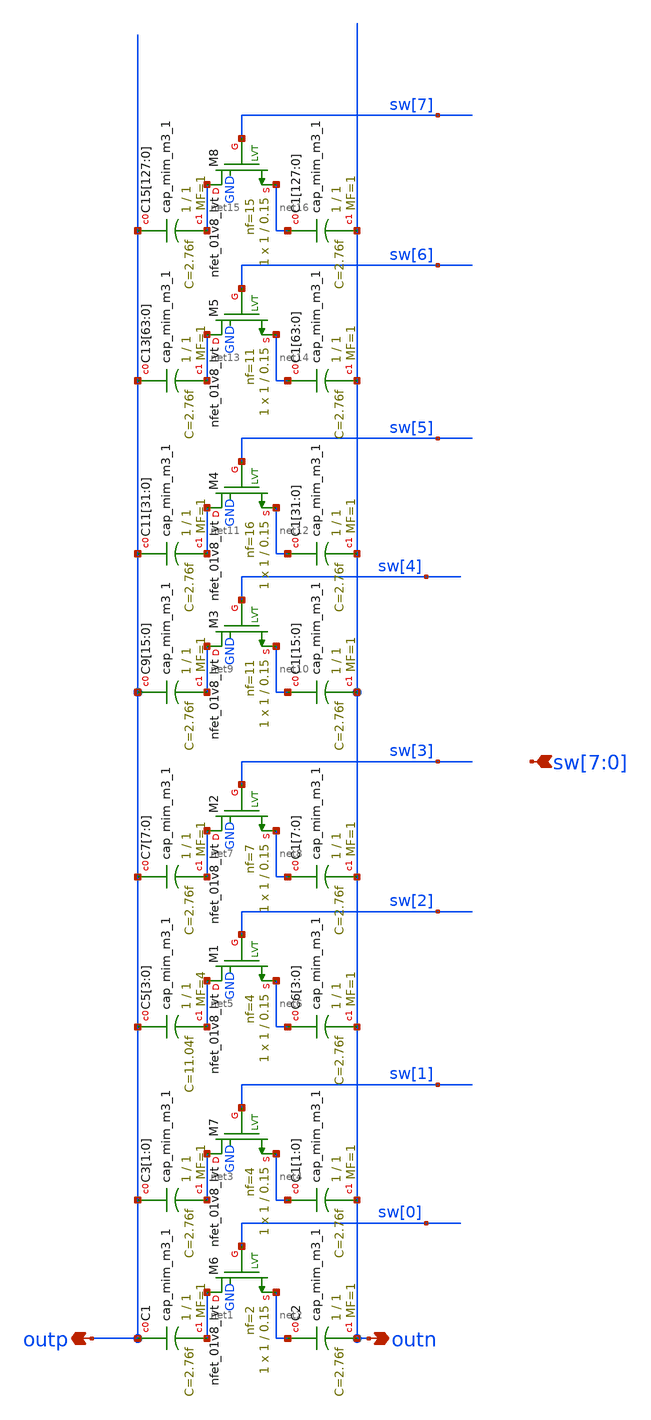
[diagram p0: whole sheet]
** sch_path: generators/lc-dco/xschem_rundir/mim_1m2C.sch
**.subckt mim_1m2C outn outp sw[7],sw[6],sw[5],sw[4],sw[3],sw[2],sw[1],sw[0]
*.opin outn
*.opin outp
*.ipin sw[7],sw[6],sw[5],sw[4],sw[3],sw[2],sw[1],sw[0]
XC1 outp net1 sky130_fd_pr__cap_mim_m3_1 W=1 L=1 MF=1 m=1
XC2 net2 outn sky130_fd_pr__cap_mim_m3_1 W=1 L=1 MF=1 m=1
XM6 net1 sw[0] net2 GND sky130_fd_pr__nfet_01v8_lvt L=0.15 W=1 nf=2 ad='int((nf+1)/2) * W/nf * 0.29'
+ as='int((nf+2)/2) * W/nf * 0.29' pd='2*int((nf+1)/2) * (W/nf + 0.29)' ps='2*int((nf+2)/2) * (W/nf + 0.29)'
+ nrd='0.29 / W' nrs='0.29 / W' sa=0 sb=0 sd=0 mult=1 m=1
XC3[1] outp net3 sky130_fd_pr__cap_mim_m3_1 W=1 L=1 MF=1 m=1
XC3[0] outp net3 sky130_fd_pr__cap_mim_m3_1 W=1 L=1 MF=1 m=1
XC1[1] net4 outn sky130_fd_pr__cap_mim_m3_1 W=1 L=1 MF=1 m=1
XC1[0] net4 outn sky130_fd_pr__cap_mim_m3_1 W=1 L=1 MF=1 m=1
XM7 net3 sw[1] net4 GND sky130_fd_pr__nfet_01v8_lvt L=0.15 W=1 nf=4 ad='int((nf+1)/2) * W/nf * 0.29'
+ as='int((nf+2)/2) * W/nf * 0.29' pd='2*int((nf+1)/2) * (W/nf + 0.29)' ps='2*int((nf+2)/2) * (W/nf + 0.29)'
+ nrd='0.29 / W' nrs='0.29 / W' sa=0 sb=0 sd=0 mult=1 m=1
XC5[3] outp net5 sky130_fd_pr__cap_mim_m3_1 W=1 L=1 MF=4 m=4
XC5[2] outp net5 sky130_fd_pr__cap_mim_m3_1 W=1 L=1 MF=4 m=4
XC5[1] outp net5 sky130_fd_pr__cap_mim_m3_1 W=1 L=1 MF=4 m=4
XC5[0] outp net5 sky130_fd_pr__cap_mim_m3_1 W=1 L=1 MF=4 m=4
XC6[3] net6 outn sky130_fd_pr__cap_mim_m3_1 W=1 L=1 MF=1 m=1
XC6[2] net6 outn sky130_fd_pr__cap_mim_m3_1 W=1 L=1 MF=1 m=1
XC6[1] net6 outn sky130_fd_pr__cap_mim_m3_1 W=1 L=1 MF=1 m=1
XC6[0] net6 outn sky130_fd_pr__cap_mim_m3_1 W=1 L=1 MF=1 m=1
XM1 net5 sw[2] net6 GND sky130_fd_pr__nfet_01v8_lvt L=0.15 W=1 nf=4 ad='int((nf+1)/2) * W/nf * 0.29'
+ as='int((nf+2)/2) * W/nf * 0.29' pd='2*int((nf+1)/2) * (W/nf + 0.29)' ps='2*int((nf+2)/2) * (W/nf + 0.29)'
+ nrd='0.29 / W' nrs='0.29 / W' sa=0 sb=0 sd=0 mult=1 m=1
XC7[7] outp net7 sky130_fd_pr__cap_mim_m3_1 W=1 L=1 MF=1 m=1
XC7[6] outp net7 sky130_fd_pr__cap_mim_m3_1 W=1 L=1 MF=1 m=1
XC7[5] outp net7 sky130_fd_pr__cap_mim_m3_1 W=1 L=1 MF=1 m=1
XC7[4] outp net7 sky130_fd_pr__cap_mim_m3_1 W=1 L=1 MF=1 m=1
XC7[3] outp net7 sky130_fd_pr__cap_mim_m3_1 W=1 L=1 MF=1 m=1
XC7[2] outp net7 sky130_fd_pr__cap_mim_m3_1 W=1 L=1 MF=1 m=1
XC7[1] outp net7 sky130_fd_pr__cap_mim_m3_1 W=1 L=1 MF=1 m=1
XC7[0] outp net7 sky130_fd_pr__cap_mim_m3_1 W=1 L=1 MF=1 m=1
XC1[7] net8 outn sky130_fd_pr__cap_mim_m3_1 W=1 L=1 MF=1 m=1
XC1[6] net8 outn sky130_fd_pr__cap_mim_m3_1 W=1 L=1 MF=1 m=1
XC1[5] net8 outn sky130_fd_pr__cap_mim_m3_1 W=1 L=1 MF=1 m=1
XC1[4] net8 outn sky130_fd_pr__cap_mim_m3_1 W=1 L=1 MF=1 m=1
XC1[3] net8 outn sky130_fd_pr__cap_mim_m3_1 W=1 L=1 MF=1 m=1
XC1[2] net8 outn sky130_fd_pr__cap_mim_m3_1 W=1 L=1 MF=1 m=1
XC1[1] net8 outn sky130_fd_pr__cap_mim_m3_1 W=1 L=1 MF=1 m=1
XC1[0] net8 outn sky130_fd_pr__cap_mim_m3_1 W=1 L=1 MF=1 m=1
XM2 net7 sw[3] net8 GND sky130_fd_pr__nfet_01v8_lvt L=0.15 W=1 nf=7 ad='int((nf+1)/2) * W/nf * 0.29'
+ as='int((nf+2)/2) * W/nf * 0.29' pd='2*int((nf+1)/2) * (W/nf + 0.29)' ps='2*int((nf+2)/2) * (W/nf + 0.29)'
+ nrd='0.29 / W' nrs='0.29 / W' sa=0 sb=0 sd=0 mult=1 m=1
XC9[15] outp net9 sky130_fd_pr__cap_mim_m3_1 W=1 L=1 MF=1 m=1
XC9[14] outp net9 sky130_fd_pr__cap_mim_m3_1 W=1 L=1 MF=1 m=1
XC9[13] outp net9 sky130_fd_pr__cap_mim_m3_1 W=1 L=1 MF=1 m=1
XC9[12] outp net9 sky130_fd_pr__cap_mim_m3_1 W=1 L=1 MF=1 m=1
XC9[11] outp net9 sky130_fd_pr__cap_mim_m3_1 W=1 L=1 MF=1 m=1
XC9[10] outp net9 sky130_fd_pr__cap_mim_m3_1 W=1 L=1 MF=1 m=1
XC9[9] outp net9 sky130_fd_pr__cap_mim_m3_1 W=1 L=1 MF=1 m=1
XC9[8] outp net9 sky130_fd_pr__cap_mim_m3_1 W=1 L=1 MF=1 m=1
XC9[7] outp net9 sky130_fd_pr__cap_mim_m3_1 W=1 L=1 MF=1 m=1
XC9[6] outp net9 sky130_fd_pr__cap_mim_m3_1 W=1 L=1 MF=1 m=1
XC9[5] outp net9 sky130_fd_pr__cap_mim_m3_1 W=1 L=1 MF=1 m=1
XC9[4] outp net9 sky130_fd_pr__cap_mim_m3_1 W=1 L=1 MF=1 m=1
XC9[3] outp net9 sky130_fd_pr__cap_mim_m3_1 W=1 L=1 MF=1 m=1
XC9[2] outp net9 sky130_fd_pr__cap_mim_m3_1 W=1 L=1 MF=1 m=1
XC9[1] outp net9 sky130_fd_pr__cap_mim_m3_1 W=1 L=1 MF=1 m=1
XC9[0] outp net9 sky130_fd_pr__cap_mim_m3_1 W=1 L=1 MF=1 m=1
XC1[15] net10 outn sky130_fd_pr__cap_mim_m3_1 W=1 L=1 MF=1 m=1
XC1[14] net10 outn sky130_fd_pr__cap_mim_m3_1 W=1 L=1 MF=1 m=1
XC1[13] net10 outn sky130_fd_pr__cap_mim_m3_1 W=1 L=1 MF=1 m=1
XC1[12] net10 outn sky130_fd_pr__cap_mim_m3_1 W=1 L=1 MF=1 m=1
XC1[11] net10 outn sky130_fd_pr__cap_mim_m3_1 W=1 L=1 MF=1 m=1
XC1[10] net10 outn sky130_fd_pr__cap_mim_m3_1 W=1 L=1 MF=1 m=1
XC1[9] net10 outn sky130_fd_pr__cap_mim_m3_1 W=1 L=1 MF=1 m=1
XC1[8] net10 outn sky130_fd_pr__cap_mim_m3_1 W=1 L=1 MF=1 m=1
XC1[7] net10 outn sky130_fd_pr__cap_mim_m3_1 W=1 L=1 MF=1 m=1
XC1[6] net10 outn sky130_fd_pr__cap_mim_m3_1 W=1 L=1 MF=1 m=1
XC1[5] net10 outn sky130_fd_pr__cap_mim_m3_1 W=1 L=1 MF=1 m=1
XC1[4] net10 outn sky130_fd_pr__cap_mim_m3_1 W=1 L=1 MF=1 m=1
XC1[3] net10 outn sky130_fd_pr__cap_mim_m3_1 W=1 L=1 MF=1 m=1
XC1[2] net10 outn sky130_fd_pr__cap_mim_m3_1 W=1 L=1 MF=1 m=1
XC1[1] net10 outn sky130_fd_pr__cap_mim_m3_1 W=1 L=1 MF=1 m=1
XC1[0] net10 outn sky130_fd_pr__cap_mim_m3_1 W=1 L=1 MF=1 m=1
XM3 net9 sw[4] net10 GND sky130_fd_pr__nfet_01v8_lvt L=0.15 W=1 nf=11 ad='int((nf+1)/2) * W/nf * 0.29'
+ as='int((nf+2)/2) * W/nf * 0.29' pd='2*int((nf+1)/2) * (W/nf + 0.29)' ps='2*int((nf+2)/2) * (W/nf + 0.29)'
+ nrd='0.29 / W' nrs='0.29 / W' sa=0 sb=0 sd=0 mult=1 m=1
XC11[31] outp net11 sky130_fd_pr__cap_mim_m3_1 W=1 L=1 MF=1 m=1
XC11[30] outp net11 sky130_fd_pr__cap_mim_m3_1 W=1 L=1 MF=1 m=1
XC11[29] outp net11 sky130_fd_pr__cap_mim_m3_1 W=1 L=1 MF=1 m=1
XC11[28] outp net11 sky130_fd_pr__cap_mim_m3_1 W=1 L=1 MF=1 m=1
XC11[27] outp net11 sky130_fd_pr__cap_mim_m3_1 W=1 L=1 MF=1 m=1
XC11[26] outp net11 sky130_fd_pr__cap_mim_m3_1 W=1 L=1 MF=1 m=1
XC11[25] outp net11 sky130_fd_pr__cap_mim_m3_1 W=1 L=1 MF=1 m=1
XC11[24] outp net11 sky130_fd_pr__cap_mim_m3_1 W=1 L=1 MF=1 m=1
XC11[23] outp net11 sky130_fd_pr__cap_mim_m3_1 W=1 L=1 MF=1 m=1
XC11[22] outp net11 sky130_fd_pr__cap_mim_m3_1 W=1 L=1 MF=1 m=1
XC11[21] outp net11 sky130_fd_pr__cap_mim_m3_1 W=1 L=1 MF=1 m=1
XC11[20] outp net11 sky130_fd_pr__cap_mim_m3_1 W=1 L=1 MF=1 m=1
XC11[19] outp net11 sky130_fd_pr__cap_mim_m3_1 W=1 L=1 MF=1 m=1
XC11[18] outp net11 sky130_fd_pr__cap_mim_m3_1 W=1 L=1 MF=1 m=1
XC11[17] outp net11 sky130_fd_pr__cap_mim_m3_1 W=1 L=1 MF=1 m=1
XC11[16] outp net11 sky130_fd_pr__cap_mim_m3_1 W=1 L=1 MF=1 m=1
XC11[15] outp net11 sky130_fd_pr__cap_mim_m3_1 W=1 L=1 MF=1 m=1
XC11[14] outp net11 sky130_fd_pr__cap_mim_m3_1 W=1 L=1 MF=1 m=1
XC11[13] outp net11 sky130_fd_pr__cap_mim_m3_1 W=1 L=1 MF=1 m=1
XC11[12] outp net11 sky130_fd_pr__cap_mim_m3_1 W=1 L=1 MF=1 m=1
XC11[11] outp net11 sky130_fd_pr__cap_mim_m3_1 W=1 L=1 MF=1 m=1
XC11[10] outp net11 sky130_fd_pr__cap_mim_m3_1 W=1 L=1 MF=1 m=1
XC11[9] outp net11 sky130_fd_pr__cap_mim_m3_1 W=1 L=1 MF=1 m=1
XC11[8] outp net11 sky130_fd_pr__cap_mim_m3_1 W=1 L=1 MF=1 m=1
XC11[7] outp net11 sky130_fd_pr__cap_mim_m3_1 W=1 L=1 MF=1 m=1
XC11[6] outp net11 sky130_fd_pr__cap_mim_m3_1 W=1 L=1 MF=1 m=1
XC11[5] outp net11 sky130_fd_pr__cap_mim_m3_1 W=1 L=1 MF=1 m=1
XC11[4] outp net11 sky130_fd_pr__cap_mim_m3_1 W=1 L=1 MF=1 m=1
XC11[3] outp net11 sky130_fd_pr__cap_mim_m3_1 W=1 L=1 MF=1 m=1
XC11[2] outp net11 sky130_fd_pr__cap_mim_m3_1 W=1 L=1 MF=1 m=1
XC11[1] outp net11 sky130_fd_pr__cap_mim_m3_1 W=1 L=1 MF=1 m=1
XC11[0] outp net11 sky130_fd_pr__cap_mim_m3_1 W=1 L=1 MF=1 m=1
XC1[31] net12 outn sky130_fd_pr__cap_mim_m3_1 W=1 L=1 MF=1 m=1
XC1[30] net12 outn sky130_fd_pr__cap_mim_m3_1 W=1 L=1 MF=1 m=1
XC1[29] net12 outn sky130_fd_pr__cap_mim_m3_1 W=1 L=1 MF=1 m=1
XC1[28] net12 outn sky130_fd_pr__cap_mim_m3_1 W=1 L=1 MF=1 m=1
XC1[27] net12 outn sky130_fd_pr__cap_mim_m3_1 W=1 L=1 MF=1 m=1
XC1[26] net12 outn sky130_fd_pr__cap_mim_m3_1 W=1 L=1 MF=1 m=1
XC1[25] net12 outn sky130_fd_pr__cap_mim_m3_1 W=1 L=1 MF=1 m=1
XC1[24] net12 outn sky130_fd_pr__cap_mim_m3_1 W=1 L=1 MF=1 m=1
XC1[23] net12 outn sky130_fd_pr__cap_mim_m3_1 W=1 L=1 MF=1 m=1
XC1[22] net12 outn sky130_fd_pr__cap_mim_m3_1 W=1 L=1 MF=1 m=1
XC1[21] net12 outn sky130_fd_pr__cap_mim_m3_1 W=1 L=1 MF=1 m=1
XC1[20] net12 outn sky130_fd_pr__cap_mim_m3_1 W=1 L=1 MF=1 m=1
XC1[19] net12 outn sky130_fd_pr__cap_mim_m3_1 W=1 L=1 MF=1 m=1
XC1[18] net12 outn sky130_fd_pr__cap_mim_m3_1 W=1 L=1 MF=1 m=1
XC1[17] net12 outn sky130_fd_pr__cap_mim_m3_1 W=1 L=1 MF=1 m=1
XC1[16] net12 outn sky130_fd_pr__cap_mim_m3_1 W=1 L=1 MF=1 m=1
XC1[15] net12 outn sky130_fd_pr__cap_mim_m3_1 W=1 L=1 MF=1 m=1
XC1[14] net12 outn sky130_fd_pr__cap_mim_m3_1 W=1 L=1 MF=1 m=1
XC1[13] net12 outn sky130_fd_pr__cap_mim_m3_1 W=1 L=1 MF=1 m=1
XC1[12] net12 outn sky130_fd_pr__cap_mim_m3_1 W=1 L=1 MF=1 m=1
XC1[11] net12 outn sky130_fd_pr__cap_mim_m3_1 W=1 L=1 MF=1 m=1
XC1[10] net12 outn sky130_fd_pr__cap_mim_m3_1 W=1 L=1 MF=1 m=1
XC1[9] net12 outn sky130_fd_pr__cap_mim_m3_1 W=1 L=1 MF=1 m=1
XC1[8] net12 outn sky130_fd_pr__cap_mim_m3_1 W=1 L=1 MF=1 m=1
XC1[7] net12 outn sky130_fd_pr__cap_mim_m3_1 W=1 L=1 MF=1 m=1
XC1[6] net12 outn sky130_fd_pr__cap_mim_m3_1 W=1 L=1 MF=1 m=1
XC1[5] net12 outn sky130_fd_pr__cap_mim_m3_1 W=1 L=1 MF=1 m=1
XC1[4] net12 outn sky130_fd_pr__cap_mim_m3_1 W=1 L=1 MF=1 m=1
XC1[3] net12 outn sky130_fd_pr__cap_mim_m3_1 W=1 L=1 MF=1 m=1
XC1[2] net12 outn sky130_fd_pr__cap_mim_m3_1 W=1 L=1 MF=1 m=1
XC1[1] net12 outn sky130_fd_pr__cap_mim_m3_1 W=1 L=1 MF=1 m=1
XC1[0] net12 outn sky130_fd_pr__cap_mim_m3_1 W=1 L=1 MF=1 m=1
XM4 net11 sw[5] net12 GND sky130_fd_pr__nfet_01v8_lvt L=0.15 W=1 nf=16 ad='int((nf+1)/2) * W/nf * 0.29'
+ as='int((nf+2)/2) * W/nf * 0.29' pd='2*int((nf+1)/2) * (W/nf + 0.29)' ps='2*int((nf+2)/2) * (W/nf + 0.29)'
+ nrd='0.29 / W' nrs='0.29 / W' sa=0 sb=0 sd=0 mult=1 m=1
XC13[63] outp net13 sky130_fd_pr__cap_mim_m3_1 W=1 L=1 MF=1 m=1
XC13[62] outp net13 sky130_fd_pr__cap_mim_m3_1 W=1 L=1 MF=1 m=1
XC13[61] outp net13 sky130_fd_pr__cap_mim_m3_1 W=1 L=1 MF=1 m=1
XC13[60] outp net13 sky130_fd_pr__cap_mim_m3_1 W=1 L=1 MF=1 m=1
XC13[59] outp net13 sky130_fd_pr__cap_mim_m3_1 W=1 L=1 MF=1 m=1
XC13[58] outp net13 sky130_fd_pr__cap_mim_m3_1 W=1 L=1 MF=1 m=1
XC13[57] outp net13 sky130_fd_pr__cap_mim_m3_1 W=1 L=1 MF=1 m=1
XC13[56] outp net13 sky130_fd_pr__cap_mim_m3_1 W=1 L=1 MF=1 m=1
XC13[55] outp net13 sky130_fd_pr__cap_mim_m3_1 W=1 L=1 MF=1 m=1
XC13[54] outp net13 sky130_fd_pr__cap_mim_m3_1 W=1 L=1 MF=1 m=1
XC13[53] outp net13 sky130_fd_pr__cap_mim_m3_1 W=1 L=1 MF=1 m=1
XC13[52] outp net13 sky130_fd_pr__cap_mim_m3_1 W=1 L=1 MF=1 m=1
XC13[51] outp net13 sky130_fd_pr__cap_mim_m3_1 W=1 L=1 MF=1 m=1
XC13[50] outp net13 sky130_fd_pr__cap_mim_m3_1 W=1 L=1 MF=1 m=1
XC13[49] outp net13 sky130_fd_pr__cap_mim_m3_1 W=1 L=1 MF=1 m=1
XC13[48] outp net13 sky130_fd_pr__cap_mim_m3_1 W=1 L=1 MF=1 m=1
XC13[47] outp net13 sky130_fd_pr__cap_mim_m3_1 W=1 L=1 MF=1 m=1
XC13[46] outp net13 sky130_fd_pr__cap_mim_m3_1 W=1 L=1 MF=1 m=1
XC13[45] outp net13 sky130_fd_pr__cap_mim_m3_1 W=1 L=1 MF=1 m=1
XC13[44] outp net13 sky130_fd_pr__cap_mim_m3_1 W=1 L=1 MF=1 m=1
XC13[43] outp net13 sky130_fd_pr__cap_mim_m3_1 W=1 L=1 MF=1 m=1
XC13[42] outp net13 sky130_fd_pr__cap_mim_m3_1 W=1 L=1 MF=1 m=1
XC13[41] outp net13 sky130_fd_pr__cap_mim_m3_1 W=1 L=1 MF=1 m=1
XC13[40] outp net13 sky130_fd_pr__cap_mim_m3_1 W=1 L=1 MF=1 m=1
XC13[39] outp net13 sky130_fd_pr__cap_mim_m3_1 W=1 L=1 MF=1 m=1
XC13[38] outp net13 sky130_fd_pr__cap_mim_m3_1 W=1 L=1 MF=1 m=1
XC13[37] outp net13 sky130_fd_pr__cap_mim_m3_1 W=1 L=1 MF=1 m=1
XC13[36] outp net13 sky130_fd_pr__cap_mim_m3_1 W=1 L=1 MF=1 m=1
XC13[35] outp net13 sky130_fd_pr__cap_mim_m3_1 W=1 L=1 MF=1 m=1
XC13[34] outp net13 sky130_fd_pr__cap_mim_m3_1 W=1 L=1 MF=1 m=1
XC13[33] outp net13 sky130_fd_pr__cap_mim_m3_1 W=1 L=1 MF=1 m=1
XC13[32] outp net13 sky130_fd_pr__cap_mim_m3_1 W=1 L=1 MF=1 m=1
XC13[31] outp net13 sky130_fd_pr__cap_mim_m3_1 W=1 L=1 MF=1 m=1
XC13[30] outp net13 sky130_fd_pr__cap_mim_m3_1 W=1 L=1 MF=1 m=1
XC13[29] outp net13 sky130_fd_pr__cap_mim_m3_1 W=1 L=1 MF=1 m=1
XC13[28] outp net13 sky130_fd_pr__cap_mim_m3_1 W=1 L=1 MF=1 m=1
XC13[27] outp net13 sky130_fd_pr__cap_mim_m3_1 W=1 L=1 MF=1 m=1
XC13[26] outp net13 sky130_fd_pr__cap_mim_m3_1 W=1 L=1 MF=1 m=1
XC13[25] outp net13 sky130_fd_pr__cap_mim_m3_1 W=1 L=1 MF=1 m=1
XC13[24] outp net13 sky130_fd_pr__cap_mim_m3_1 W=1 L=1 MF=1 m=1
XC13[23] outp net13 sky130_fd_pr__cap_mim_m3_1 W=1 L=1 MF=1 m=1
XC13[22] outp net13 sky130_fd_pr__cap_mim_m3_1 W=1 L=1 MF=1 m=1
XC13[21] outp net13 sky130_fd_pr__cap_mim_m3_1 W=1 L=1 MF=1 m=1
XC13[20] outp net13 sky130_fd_pr__cap_mim_m3_1 W=1 L=1 MF=1 m=1
XC13[19] outp net13 sky130_fd_pr__cap_mim_m3_1 W=1 L=1 MF=1 m=1
XC13[18] outp net13 sky130_fd_pr__cap_mim_m3_1 W=1 L=1 MF=1 m=1
XC13[17] outp net13 sky130_fd_pr__cap_mim_m3_1 W=1 L=1 MF=1 m=1
XC13[16] outp net13 sky130_fd_pr__cap_mim_m3_1 W=1 L=1 MF=1 m=1
XC13[15] outp net13 sky130_fd_pr__cap_mim_m3_1 W=1 L=1 MF=1 m=1
XC13[14] outp net13 sky130_fd_pr__cap_mim_m3_1 W=1 L=1 MF=1 m=1
XC13[13] outp net13 sky130_fd_pr__cap_mim_m3_1 W=1 L=1 MF=1 m=1
XC13[12] outp net13 sky130_fd_pr__cap_mim_m3_1 W=1 L=1 MF=1 m=1
XC13[11] outp net13 sky130_fd_pr__cap_mim_m3_1 W=1 L=1 MF=1 m=1
XC13[10] outp net13 sky130_fd_pr__cap_mim_m3_1 W=1 L=1 MF=1 m=1
XC13[9] outp net13 sky130_fd_pr__cap_mim_m3_1 W=1 L=1 MF=1 m=1
XC13[8] outp net13 sky130_fd_pr__cap_mim_m3_1 W=1 L=1 MF=1 m=1
XC13[7] outp net13 sky130_fd_pr__cap_mim_m3_1 W=1 L=1 MF=1 m=1
XC13[6] outp net13 sky130_fd_pr__cap_mim_m3_1 W=1 L=1 MF=1 m=1
XC13[5] outp net13 sky130_fd_pr__cap_mim_m3_1 W=1 L=1 MF=1 m=1
XC13[4] outp net13 sky130_fd_pr__cap_mim_m3_1 W=1 L=1 MF=1 m=1
XC13[3] outp net13 sky130_fd_pr__cap_mim_m3_1 W=1 L=1 MF=1 m=1
XC13[2] outp net13 sky130_fd_pr__cap_mim_m3_1 W=1 L=1 MF=1 m=1
XC13[1] outp net13 sky130_fd_pr__cap_mim_m3_1 W=1 L=1 MF=1 m=1
XC13[0] outp net13 sky130_fd_pr__cap_mim_m3_1 W=1 L=1 MF=1 m=1
XC1[63] net14 outn sky130_fd_pr__cap_mim_m3_1 W=1 L=1 MF=1 m=1
XC1[62] net14 outn sky130_fd_pr__cap_mim_m3_1 W=1 L=1 MF=1 m=1
XC1[61] net14 outn sky130_fd_pr__cap_mim_m3_1 W=1 L=1 MF=1 m=1
XC1[60] net14 outn sky130_fd_pr__cap_mim_m3_1 W=1 L=1 MF=1 m=1
XC1[59] net14 outn sky130_fd_pr__cap_mim_m3_1 W=1 L=1 MF=1 m=1
XC1[58] net14 outn sky130_fd_pr__cap_mim_m3_1 W=1 L=1 MF=1 m=1
XC1[57] net14 outn sky130_fd_pr__cap_mim_m3_1 W=1 L=1 MF=1 m=1
XC1[56] net14 outn sky130_fd_pr__cap_mim_m3_1 W=1 L=1 MF=1 m=1
XC1[55] net14 outn sky130_fd_pr__cap_mim_m3_1 W=1 L=1 MF=1 m=1
XC1[54] net14 outn sky130_fd_pr__cap_mim_m3_1 W=1 L=1 MF=1 m=1
XC1[53] net14 outn sky130_fd_pr__cap_mim_m3_1 W=1 L=1 MF=1 m=1
XC1[52] net14 outn sky130_fd_pr__cap_mim_m3_1 W=1 L=1 MF=1 m=1
XC1[51] net14 outn sky130_fd_pr__cap_mim_m3_1 W=1 L=1 MF=1 m=1
XC1[50] net14 outn sky130_fd_pr__cap_mim_m3_1 W=1 L=1 MF=1 m=1
XC1[49] net14 outn sky130_fd_pr__cap_mim_m3_1 W=1 L=1 MF=1 m=1
XC1[48] net14 outn sky130_fd_pr__cap_mim_m3_1 W=1 L=1 MF=1 m=1
XC1[47] net14 outn sky130_fd_pr__cap_mim_m3_1 W=1 L=1 MF=1 m=1
XC1[46] net14 outn sky130_fd_pr__cap_mim_m3_1 W=1 L=1 MF=1 m=1
XC1[45] net14 outn sky130_fd_pr__cap_mim_m3_1 W=1 L=1 MF=1 m=1
XC1[44] net14 outn sky130_fd_pr__cap_mim_m3_1 W=1 L=1 MF=1 m=1
XC1[43] net14 outn sky130_fd_pr__cap_mim_m3_1 W=1 L=1 MF=1 m=1
XC1[42] net14 outn sky130_fd_pr__cap_mim_m3_1 W=1 L=1 MF=1 m=1
XC1[41] net14 outn sky130_fd_pr__cap_mim_m3_1 W=1 L=1 MF=1 m=1
XC1[40] net14 outn sky130_fd_pr__cap_mim_m3_1 W=1 L=1 MF=1 m=1
XC1[39] net14 outn sky130_fd_pr__cap_mim_m3_1 W=1 L=1 MF=1 m=1
XC1[38] net14 outn sky130_fd_pr__cap_mim_m3_1 W=1 L=1 MF=1 m=1
XC1[37] net14 outn sky130_fd_pr__cap_mim_m3_1 W=1 L=1 MF=1 m=1
XC1[36] net14 outn sky130_fd_pr__cap_mim_m3_1 W=1 L=1 MF=1 m=1
XC1[35] net14 outn sky130_fd_pr__cap_mim_m3_1 W=1 L=1 MF=1 m=1
XC1[34] net14 outn sky130_fd_pr__cap_mim_m3_1 W=1 L=1 MF=1 m=1
XC1[33] net14 outn sky130_fd_pr__cap_mim_m3_1 W=1 L=1 MF=1 m=1
XC1[32] net14 outn sky130_fd_pr__cap_mim_m3_1 W=1 L=1 MF=1 m=1
XC1[31] net14 outn sky130_fd_pr__cap_mim_m3_1 W=1 L=1 MF=1 m=1
XC1[30] net14 outn sky130_fd_pr__cap_mim_m3_1 W=1 L=1 MF=1 m=1
XC1[29] net14 outn sky130_fd_pr__cap_mim_m3_1 W=1 L=1 MF=1 m=1
XC1[28] net14 outn sky130_fd_pr__cap_mim_m3_1 W=1 L=1 MF=1 m=1
XC1[27] net14 outn sky130_fd_pr__cap_mim_m3_1 W=1 L=1 MF=1 m=1
XC1[26] net14 outn sky130_fd_pr__cap_mim_m3_1 W=1 L=1 MF=1 m=1
XC1[25] net14 outn sky130_fd_pr__cap_mim_m3_1 W=1 L=1 MF=1 m=1
XC1[24] net14 outn sky130_fd_pr__cap_mim_m3_1 W=1 L=1 MF=1 m=1
XC1[23] net14 outn sky130_fd_pr__cap_mim_m3_1 W=1 L=1 MF=1 m=1
XC1[22] net14 outn sky130_fd_pr__cap_mim_m3_1 W=1 L=1 MF=1 m=1
XC1[21] net14 outn sky130_fd_pr__cap_mim_m3_1 W=1 L=1 MF=1 m=1
XC1[20] net14 outn sky130_fd_pr__cap_mim_m3_1 W=1 L=1 MF=1 m=1
XC1[19] net14 outn sky130_fd_pr__cap_mim_m3_1 W=1 L=1 MF=1 m=1
XC1[18] net14 outn sky130_fd_pr__cap_mim_m3_1 W=1 L=1 MF=1 m=1
XC1[17] net14 outn sky130_fd_pr__cap_mim_m3_1 W=1 L=1 MF=1 m=1
XC1[16] net14 outn sky130_fd_pr__cap_mim_m3_1 W=1 L=1 MF=1 m=1
XC1[15] net14 outn sky130_fd_pr__cap_mim_m3_1 W=1 L=1 MF=1 m=1
XC1[14] net14 outn sky130_fd_pr__cap_mim_m3_1 W=1 L=1 MF=1 m=1
XC1[13] net14 outn sky130_fd_pr__cap_mim_m3_1 W=1 L=1 MF=1 m=1
XC1[12] net14 outn sky130_fd_pr__cap_mim_m3_1 W=1 L=1 MF=1 m=1
XC1[11] net14 outn sky130_fd_pr__cap_mim_m3_1 W=1 L=1 MF=1 m=1
XC1[10] net14 outn sky130_fd_pr__cap_mim_m3_1 W=1 L=1 MF=1 m=1
XC1[9] net14 outn sky130_fd_pr__cap_mim_m3_1 W=1 L=1 MF=1 m=1
XC1[8] net14 outn sky130_fd_pr__cap_mim_m3_1 W=1 L=1 MF=1 m=1
XC1[7] net14 outn sky130_fd_pr__cap_mim_m3_1 W=1 L=1 MF=1 m=1
XC1[6] net14 outn sky130_fd_pr__cap_mim_m3_1 W=1 L=1 MF=1 m=1
XC1[5] net14 outn sky130_fd_pr__cap_mim_m3_1 W=1 L=1 MF=1 m=1
XC1[4] net14 outn sky130_fd_pr__cap_mim_m3_1 W=1 L=1 MF=1 m=1
XC1[3] net14 outn sky130_fd_pr__cap_mim_m3_1 W=1 L=1 MF=1 m=1
XC1[2] net14 outn sky130_fd_pr__cap_mim_m3_1 W=1 L=1 MF=1 m=1
XC1[1] net14 outn sky130_fd_pr__cap_mim_m3_1 W=1 L=1 MF=1 m=1
XC1[0] net14 outn sky130_fd_pr__cap_mim_m3_1 W=1 L=1 MF=1 m=1
XM5 net13 sw[6] net14 GND sky130_fd_pr__nfet_01v8_lvt L=0.15 W=1 nf=11 ad='int((nf+1)/2) * W/nf * 0.29'
+ as='int((nf+2)/2) * W/nf * 0.29' pd='2*int((nf+1)/2) * (W/nf + 0.29)' ps='2*int((nf+2)/2) * (W/nf + 0.29)'
+ nrd='0.29 / W' nrs='0.29 / W' sa=0 sb=0 sd=0 mult=1 m=1
XC15[127] outp net15 sky130_fd_pr__cap_mim_m3_1 W=1 L=1 MF=1 m=1
XC15[126] outp net15 sky130_fd_pr__cap_mim_m3_1 W=1 L=1 MF=1 m=1
XC15[125] outp net15 sky130_fd_pr__cap_mim_m3_1 W=1 L=1 MF=1 m=1
XC15[124] outp net15 sky130_fd_pr__cap_mim_m3_1 W=1 L=1 MF=1 m=1
XC15[123] outp net15 sky130_fd_pr__cap_mim_m3_1 W=1 L=1 MF=1 m=1
XC15[122] outp net15 sky130_fd_pr__cap_mim_m3_1 W=1 L=1 MF=1 m=1
XC15[121] outp net15 sky130_fd_pr__cap_mim_m3_1 W=1 L=1 MF=1 m=1
XC15[120] outp net15 sky130_fd_pr__cap_mim_m3_1 W=1 L=1 MF=1 m=1
XC15[119] outp net15 sky130_fd_pr__cap_mim_m3_1 W=1 L=1 MF=1 m=1
XC15[118] outp net15 sky130_fd_pr__cap_mim_m3_1 W=1 L=1 MF=1 m=1
XC15[117] outp net15 sky130_fd_pr__cap_mim_m3_1 W=1 L=1 MF=1 m=1
XC15[116] outp net15 sky130_fd_pr__cap_mim_m3_1 W=1 L=1 MF=1 m=1
XC15[115] outp net15 sky130_fd_pr__cap_mim_m3_1 W=1 L=1 MF=1 m=1
XC15[114] outp net15 sky130_fd_pr__cap_mim_m3_1 W=1 L=1 MF=1 m=1
XC15[113] outp net15 sky130_fd_pr__cap_mim_m3_1 W=1 L=1 MF=1 m=1
XC15[112] outp net15 sky130_fd_pr__cap_mim_m3_1 W=1 L=1 MF=1 m=1
XC15[111] outp net15 sky130_fd_pr__cap_mim_m3_1 W=1 L=1 MF=1 m=1
XC15[110] outp net15 sky130_fd_pr__cap_mim_m3_1 W=1 L=1 MF=1 m=1
XC15[109] outp net15 sky130_fd_pr__cap_mim_m3_1 W=1 L=1 MF=1 m=1
XC15[108] outp net15 sky130_fd_pr__cap_mim_m3_1 W=1 L=1 MF=1 m=1
XC15[107] outp net15 sky130_fd_pr__cap_mim_m3_1 W=1 L=1 MF=1 m=1
XC15[106] outp net15 sky130_fd_pr__cap_mim_m3_1 W=1 L=1 MF=1 m=1
XC15[105] outp net15 sky130_fd_pr__cap_mim_m3_1 W=1 L=1 MF=1 m=1
XC15[104] outp net15 sky130_fd_pr__cap_mim_m3_1 W=1 L=1 MF=1 m=1
XC15[103] outp net15 sky130_fd_pr__cap_mim_m3_1 W=1 L=1 MF=1 m=1
XC15[102] outp net15 sky130_fd_pr__cap_mim_m3_1 W=1 L=1 MF=1 m=1
XC15[101] outp net15 sky130_fd_pr__cap_mim_m3_1 W=1 L=1 MF=1 m=1
XC15[100] outp net15 sky130_fd_pr__cap_mim_m3_1 W=1 L=1 MF=1 m=1
XC15[99] outp net15 sky130_fd_pr__cap_mim_m3_1 W=1 L=1 MF=1 m=1
XC15[98] outp net15 sky130_fd_pr__cap_mim_m3_1 W=1 L=1 MF=1 m=1
XC15[97] outp net15 sky130_fd_pr__cap_mim_m3_1 W=1 L=1 MF=1 m=1
XC15[96] outp net15 sky130_fd_pr__cap_mim_m3_1 W=1 L=1 MF=1 m=1
XC15[95] outp net15 sky130_fd_pr__cap_mim_m3_1 W=1 L=1 MF=1 m=1
XC15[94] outp net15 sky130_fd_pr__cap_mim_m3_1 W=1 L=1 MF=1 m=1
XC15[93] outp net15 sky130_fd_pr__cap_mim_m3_1 W=1 L=1 MF=1 m=1
XC15[92] outp net15 sky130_fd_pr__cap_mim_m3_1 W=1 L=1 MF=1 m=1
XC15[91] outp net15 sky130_fd_pr__cap_mim_m3_1 W=1 L=1 MF=1 m=1
XC15[90] outp net15 sky130_fd_pr__cap_mim_m3_1 W=1 L=1 MF=1 m=1
XC15[89] outp net15 sky130_fd_pr__cap_mim_m3_1 W=1 L=1 MF=1 m=1
XC15[88] outp net15 sky130_fd_pr__cap_mim_m3_1 W=1 L=1 MF=1 m=1
XC15[87] outp net15 sky130_fd_pr__cap_mim_m3_1 W=1 L=1 MF=1 m=1
XC15[86] outp net15 sky130_fd_pr__cap_mim_m3_1 W=1 L=1 MF=1 m=1
XC15[85] outp net15 sky130_fd_pr__cap_mim_m3_1 W=1 L=1 MF=1 m=1
XC15[84] outp net15 sky130_fd_pr__cap_mim_m3_1 W=1 L=1 MF=1 m=1
XC15[83] outp net15 sky130_fd_pr__cap_mim_m3_1 W=1 L=1 MF=1 m=1
XC15[82] outp net15 sky130_fd_pr__cap_mim_m3_1 W=1 L=1 MF=1 m=1
XC15[81] outp net15 sky130_fd_pr__cap_mim_m3_1 W=1 L=1 MF=1 m=1
XC15[80] outp net15 sky130_fd_pr__cap_mim_m3_1 W=1 L=1 MF=1 m=1
XC15[79] outp net15 sky130_fd_pr__cap_mim_m3_1 W=1 L=1 MF=1 m=1
XC15[78] outp net15 sky130_fd_pr__cap_mim_m3_1 W=1 L=1 MF=1 m=1
XC15[77] outp net15 sky130_fd_pr__cap_mim_m3_1 W=1 L=1 MF=1 m=1
XC15[76] outp net15 sky130_fd_pr__cap_mim_m3_1 W=1 L=1 MF=1 m=1
XC15[75] outp net15 sky130_fd_pr__cap_mim_m3_1 W=1 L=1 MF=1 m=1
XC15[74] outp net15 sky130_fd_pr__cap_mim_m3_1 W=1 L=1 MF=1 m=1
XC15[73] outp net15 sky130_fd_pr__cap_mim_m3_1 W=1 L=1 MF=1 m=1
XC15[72] outp net15 sky130_fd_pr__cap_mim_m3_1 W=1 L=1 MF=1 m=1
XC15[71] outp net15 sky130_fd_pr__cap_mim_m3_1 W=1 L=1 MF=1 m=1
XC15[70] outp net15 sky130_fd_pr__cap_mim_m3_1 W=1 L=1 MF=1 m=1
XC15[69] outp net15 sky130_fd_pr__cap_mim_m3_1 W=1 L=1 MF=1 m=1
XC15[68] outp net15 sky130_fd_pr__cap_mim_m3_1 W=1 L=1 MF=1 m=1
XC15[67] outp net15 sky130_fd_pr__cap_mim_m3_1 W=1 L=1 MF=1 m=1
XC15[66] outp net15 sky130_fd_pr__cap_mim_m3_1 W=1 L=1 MF=1 m=1
XC15[65] outp net15 sky130_fd_pr__cap_mim_m3_1 W=1 L=1 MF=1 m=1
XC15[64] outp net15 sky130_fd_pr__cap_mim_m3_1 W=1 L=1 MF=1 m=1
XC15[63] outp net15 sky130_fd_pr__cap_mim_m3_1 W=1 L=1 MF=1 m=1
XC15[62] outp net15 sky130_fd_pr__cap_mim_m3_1 W=1 L=1 MF=1 m=1
XC15[61] outp net15 sky130_fd_pr__cap_mim_m3_1 W=1 L=1 MF=1 m=1
XC15[60] outp net15 sky130_fd_pr__cap_mim_m3_1 W=1 L=1 MF=1 m=1
XC15[59] outp net15 sky130_fd_pr__cap_mim_m3_1 W=1 L=1 MF=1 m=1
XC15[58] outp net15 sky130_fd_pr__cap_mim_m3_1 W=1 L=1 MF=1 m=1
XC15[57] outp net15 sky130_fd_pr__cap_mim_m3_1 W=1 L=1 MF=1 m=1
XC15[56] outp net15 sky130_fd_pr__cap_mim_m3_1 W=1 L=1 MF=1 m=1
XC15[55] outp net15 sky130_fd_pr__cap_mim_m3_1 W=1 L=1 MF=1 m=1
XC15[54] outp net15 sky130_fd_pr__cap_mim_m3_1 W=1 L=1 MF=1 m=1
XC15[53] outp net15 sky130_fd_pr__cap_mim_m3_1 W=1 L=1 MF=1 m=1
XC15[52] outp net15 sky130_fd_pr__cap_mim_m3_1 W=1 L=1 MF=1 m=1
XC15[51] outp net15 sky130_fd_pr__cap_mim_m3_1 W=1 L=1 MF=1 m=1
XC15[50] outp net15 sky130_fd_pr__cap_mim_m3_1 W=1 L=1 MF=1 m=1
XC15[49] outp net15 sky130_fd_pr__cap_mim_m3_1 W=1 L=1 MF=1 m=1
XC15[48] outp net15 sky130_fd_pr__cap_mim_m3_1 W=1 L=1 MF=1 m=1
XC15[47] outp net15 sky130_fd_pr__cap_mim_m3_1 W=1 L=1 MF=1 m=1
XC15[46] outp net15 sky130_fd_pr__cap_mim_m3_1 W=1 L=1 MF=1 m=1
XC15[45] outp net15 sky130_fd_pr__cap_mim_m3_1 W=1 L=1 MF=1 m=1
XC15[44] outp net15 sky130_fd_pr__cap_mim_m3_1 W=1 L=1 MF=1 m=1
XC15[43] outp net15 sky130_fd_pr__cap_mim_m3_1 W=1 L=1 MF=1 m=1
XC15[42] outp net15 sky130_fd_pr__cap_mim_m3_1 W=1 L=1 MF=1 m=1
XC15[41] outp net15 sky130_fd_pr__cap_mim_m3_1 W=1 L=1 MF=1 m=1
XC15[40] outp net15 sky130_fd_pr__cap_mim_m3_1 W=1 L=1 MF=1 m=1
XC15[39] outp net15 sky130_fd_pr__cap_mim_m3_1 W=1 L=1 MF=1 m=1
XC15[38] outp net15 sky130_fd_pr__cap_mim_m3_1 W=1 L=1 MF=1 m=1
XC15[37] outp net15 sky130_fd_pr__cap_mim_m3_1 W=1 L=1 MF=1 m=1
XC15[36] outp net15 sky130_fd_pr__cap_mim_m3_1 W=1 L=1 MF=1 m=1
XC15[35] outp net15 sky130_fd_pr__cap_mim_m3_1 W=1 L=1 MF=1 m=1
XC15[34] outp net15 sky130_fd_pr__cap_mim_m3_1 W=1 L=1 MF=1 m=1
XC15[33] outp net15 sky130_fd_pr__cap_mim_m3_1 W=1 L=1 MF=1 m=1
XC15[32] outp net15 sky130_fd_pr__cap_mim_m3_1 W=1 L=1 MF=1 m=1
XC15[31] outp net15 sky130_fd_pr__cap_mim_m3_1 W=1 L=1 MF=1 m=1
XC15[30] outp net15 sky130_fd_pr__cap_mim_m3_1 W=1 L=1 MF=1 m=1
XC15[29] outp net15 sky130_fd_pr__cap_mim_m3_1 W=1 L=1 MF=1 m=1
XC15[28] outp net15 sky130_fd_pr__cap_mim_m3_1 W=1 L=1 MF=1 m=1
XC15[27] outp net15 sky130_fd_pr__cap_mim_m3_1 W=1 L=1 MF=1 m=1
XC15[26] outp net15 sky130_fd_pr__cap_mim_m3_1 W=1 L=1 MF=1 m=1
XC15[25] outp net15 sky130_fd_pr__cap_mim_m3_1 W=1 L=1 MF=1 m=1
XC15[24] outp net15 sky130_fd_pr__cap_mim_m3_1 W=1 L=1 MF=1 m=1
XC15[23] outp net15 sky130_fd_pr__cap_mim_m3_1 W=1 L=1 MF=1 m=1
XC15[22] outp net15 sky130_fd_pr__cap_mim_m3_1 W=1 L=1 MF=1 m=1
XC15[21] outp net15 sky130_fd_pr__cap_mim_m3_1 W=1 L=1 MF=1 m=1
XC15[20] outp net15 sky130_fd_pr__cap_mim_m3_1 W=1 L=1 MF=1 m=1
XC15[19] outp net15 sky130_fd_pr__cap_mim_m3_1 W=1 L=1 MF=1 m=1
XC15[18] outp net15 sky130_fd_pr__cap_mim_m3_1 W=1 L=1 MF=1 m=1
XC15[17] outp net15 sky130_fd_pr__cap_mim_m3_1 W=1 L=1 MF=1 m=1
XC15[16] outp net15 sky130_fd_pr__cap_mim_m3_1 W=1 L=1 MF=1 m=1
XC15[15] outp net15 sky130_fd_pr__cap_mim_m3_1 W=1 L=1 MF=1 m=1
XC15[14] outp net15 sky130_fd_pr__cap_mim_m3_1 W=1 L=1 MF=1 m=1
XC15[13] outp net15 sky130_fd_pr__cap_mim_m3_1 W=1 L=1 MF=1 m=1
XC15[12] outp net15 sky130_fd_pr__cap_mim_m3_1 W=1 L=1 MF=1 m=1
XC15[11] outp net15 sky130_fd_pr__cap_mim_m3_1 W=1 L=1 MF=1 m=1
XC15[10] outp net15 sky130_fd_pr__cap_mim_m3_1 W=1 L=1 MF=1 m=1
XC15[9] outp net15 sky130_fd_pr__cap_mim_m3_1 W=1 L=1 MF=1 m=1
XC15[8] outp net15 sky130_fd_pr__cap_mim_m3_1 W=1 L=1 MF=1 m=1
XC15[7] outp net15 sky130_fd_pr__cap_mim_m3_1 W=1 L=1 MF=1 m=1
XC15[6] outp net15 sky130_fd_pr__cap_mim_m3_1 W=1 L=1 MF=1 m=1
XC15[5] outp net15 sky130_fd_pr__cap_mim_m3_1 W=1 L=1 MF=1 m=1
XC15[4] outp net15 sky130_fd_pr__cap_mim_m3_1 W=1 L=1 MF=1 m=1
XC15[3] outp net15 sky130_fd_pr__cap_mim_m3_1 W=1 L=1 MF=1 m=1
XC15[2] outp net15 sky130_fd_pr__cap_mim_m3_1 W=1 L=1 MF=1 m=1
XC15[1] outp net15 sky130_fd_pr__cap_mim_m3_1 W=1 L=1 MF=1 m=1
XC15[0] outp net15 sky130_fd_pr__cap_mim_m3_1 W=1 L=1 MF=1 m=1
XC1[127] net16 outn sky130_fd_pr__cap_mim_m3_1 W=1 L=1 MF=1 m=1
XC1[126] net16 outn sky130_fd_pr__cap_mim_m3_1 W=1 L=1 MF=1 m=1
XC1[125] net16 outn sky130_fd_pr__cap_mim_m3_1 W=1 L=1 MF=1 m=1
XC1[124] net16 outn sky130_fd_pr__cap_mim_m3_1 W=1 L=1 MF=1 m=1
XC1[123] net16 outn sky130_fd_pr__cap_mim_m3_1 W=1 L=1 MF=1 m=1
XC1[122] net16 outn sky130_fd_pr__cap_mim_m3_1 W=1 L=1 MF=1 m=1
XC1[121] net16 outn sky130_fd_pr__cap_mim_m3_1 W=1 L=1 MF=1 m=1
XC1[120] net16 outn sky130_fd_pr__cap_mim_m3_1 W=1 L=1 MF=1 m=1
XC1[119] net16 outn sky130_fd_pr__cap_mim_m3_1 W=1 L=1 MF=1 m=1
XC1[118] net16 outn sky130_fd_pr__cap_mim_m3_1 W=1 L=1 MF=1 m=1
XC1[117] net16 outn sky130_fd_pr__cap_mim_m3_1 W=1 L=1 MF=1 m=1
XC1[116] net16 outn sky130_fd_pr__cap_mim_m3_1 W=1 L=1 MF=1 m=1
XC1[115] net16 outn sky130_fd_pr__cap_mim_m3_1 W=1 L=1 MF=1 m=1
XC1[114] net16 outn sky130_fd_pr__cap_mim_m3_1 W=1 L=1 MF=1 m=1
XC1[113] net16 outn sky130_fd_pr__cap_mim_m3_1 W=1 L=1 MF=1 m=1
XC1[112] net16 outn sky130_fd_pr__cap_mim_m3_1 W=1 L=1 MF=1 m=1
XC1[111] net16 outn sky130_fd_pr__cap_mim_m3_1 W=1 L=1 MF=1 m=1
XC1[110] net16 outn sky130_fd_pr__cap_mim_m3_1 W=1 L=1 MF=1 m=1
XC1[109] net16 outn sky130_fd_pr__cap_mim_m3_1 W=1 L=1 MF=1 m=1
XC1[108] net16 outn sky130_fd_pr__cap_mim_m3_1 W=1 L=1 MF=1 m=1
XC1[107] net16 outn sky130_fd_pr__cap_mim_m3_1 W=1 L=1 MF=1 m=1
XC1[106] net16 outn sky130_fd_pr__cap_mim_m3_1 W=1 L=1 MF=1 m=1
XC1[105] net16 outn sky130_fd_pr__cap_mim_m3_1 W=1 L=1 MF=1 m=1
XC1[104] net16 outn sky130_fd_pr__cap_mim_m3_1 W=1 L=1 MF=1 m=1
XC1[103] net16 outn sky130_fd_pr__cap_mim_m3_1 W=1 L=1 MF=1 m=1
XC1[102] net16 outn sky130_fd_pr__cap_mim_m3_1 W=1 L=1 MF=1 m=1
XC1[101] net16 outn sky130_fd_pr__cap_mim_m3_1 W=1 L=1 MF=1 m=1
XC1[100] net16 outn sky130_fd_pr__cap_mim_m3_1 W=1 L=1 MF=1 m=1
XC1[99] net16 outn sky130_fd_pr__cap_mim_m3_1 W=1 L=1 MF=1 m=1
XC1[98] net16 outn sky130_fd_pr__cap_mim_m3_1 W=1 L=1 MF=1 m=1
XC1[97] net16 outn sky130_fd_pr__cap_mim_m3_1 W=1 L=1 MF=1 m=1
XC1[96] net16 outn sky130_fd_pr__cap_mim_m3_1 W=1 L=1 MF=1 m=1
XC1[95] net16 outn sky130_fd_pr__cap_mim_m3_1 W=1 L=1 MF=1 m=1
XC1[94] net16 outn sky130_fd_pr__cap_mim_m3_1 W=1 L=1 MF=1 m=1
XC1[93] net16 outn sky130_fd_pr__cap_mim_m3_1 W=1 L=1 MF=1 m=1
XC1[92] net16 outn sky130_fd_pr__cap_mim_m3_1 W=1 L=1 MF=1 m=1
XC1[91] net16 outn sky130_fd_pr__cap_mim_m3_1 W=1 L=1 MF=1 m=1
XC1[90] net16 outn sky130_fd_pr__cap_mim_m3_1 W=1 L=1 MF=1 m=1
XC1[89] net16 outn sky130_fd_pr__cap_mim_m3_1 W=1 L=1 MF=1 m=1
XC1[88] net16 outn sky130_fd_pr__cap_mim_m3_1 W=1 L=1 MF=1 m=1
XC1[87] net16 outn sky130_fd_pr__cap_mim_m3_1 W=1 L=1 MF=1 m=1
XC1[86] net16 outn sky130_fd_pr__cap_mim_m3_1 W=1 L=1 MF=1 m=1
XC1[85] net16 outn sky130_fd_pr__cap_mim_m3_1 W=1 L=1 MF=1 m=1
XC1[84] net16 outn sky130_fd_pr__cap_mim_m3_1 W=1 L=1 MF=1 m=1
XC1[83] net16 outn sky130_fd_pr__cap_mim_m3_1 W=1 L=1 MF=1 m=1
XC1[82] net16 outn sky130_fd_pr__cap_mim_m3_1 W=1 L=1 MF=1 m=1
XC1[81] net16 outn sky130_fd_pr__cap_mim_m3_1 W=1 L=1 MF=1 m=1
XC1[80] net16 outn sky130_fd_pr__cap_mim_m3_1 W=1 L=1 MF=1 m=1
XC1[79] net16 outn sky130_fd_pr__cap_mim_m3_1 W=1 L=1 MF=1 m=1
XC1[78] net16 outn sky130_fd_pr__cap_mim_m3_1 W=1 L=1 MF=1 m=1
XC1[77] net16 outn sky130_fd_pr__cap_mim_m3_1 W=1 L=1 MF=1 m=1
XC1[76] net16 outn sky130_fd_pr__cap_mim_m3_1 W=1 L=1 MF=1 m=1
XC1[75] net16 outn sky130_fd_pr__cap_mim_m3_1 W=1 L=1 MF=1 m=1
XC1[74] net16 outn sky130_fd_pr__cap_mim_m3_1 W=1 L=1 MF=1 m=1
XC1[73] net16 outn sky130_fd_pr__cap_mim_m3_1 W=1 L=1 MF=1 m=1
XC1[72] net16 outn sky130_fd_pr__cap_mim_m3_1 W=1 L=1 MF=1 m=1
XC1[71] net16 outn sky130_fd_pr__cap_mim_m3_1 W=1 L=1 MF=1 m=1
XC1[70] net16 outn sky130_fd_pr__cap_mim_m3_1 W=1 L=1 MF=1 m=1
XC1[69] net16 outn sky130_fd_pr__cap_mim_m3_1 W=1 L=1 MF=1 m=1
XC1[68] net16 outn sky130_fd_pr__cap_mim_m3_1 W=1 L=1 MF=1 m=1
XC1[67] net16 outn sky130_fd_pr__cap_mim_m3_1 W=1 L=1 MF=1 m=1
XC1[66] net16 outn sky130_fd_pr__cap_mim_m3_1 W=1 L=1 MF=1 m=1
XC1[65] net16 outn sky130_fd_pr__cap_mim_m3_1 W=1 L=1 MF=1 m=1
XC1[64] net16 outn sky130_fd_pr__cap_mim_m3_1 W=1 L=1 MF=1 m=1
XC1[63] net16 outn sky130_fd_pr__cap_mim_m3_1 W=1 L=1 MF=1 m=1
XC1[62] net16 outn sky130_fd_pr__cap_mim_m3_1 W=1 L=1 MF=1 m=1
XC1[61] net16 outn sky130_fd_pr__cap_mim_m3_1 W=1 L=1 MF=1 m=1
XC1[60] net16 outn sky130_fd_pr__cap_mim_m3_1 W=1 L=1 MF=1 m=1
XC1[59] net16 outn sky130_fd_pr__cap_mim_m3_1 W=1 L=1 MF=1 m=1
XC1[58] net16 outn sky130_fd_pr__cap_mim_m3_1 W=1 L=1 MF=1 m=1
XC1[57] net16 outn sky130_fd_pr__cap_mim_m3_1 W=1 L=1 MF=1 m=1
XC1[56] net16 outn sky130_fd_pr__cap_mim_m3_1 W=1 L=1 MF=1 m=1
XC1[55] net16 outn sky130_fd_pr__cap_mim_m3_1 W=1 L=1 MF=1 m=1
XC1[54] net16 outn sky130_fd_pr__cap_mim_m3_1 W=1 L=1 MF=1 m=1
XC1[53] net16 outn sky130_fd_pr__cap_mim_m3_1 W=1 L=1 MF=1 m=1
XC1[52] net16 outn sky130_fd_pr__cap_mim_m3_1 W=1 L=1 MF=1 m=1
XC1[51] net16 outn sky130_fd_pr__cap_mim_m3_1 W=1 L=1 MF=1 m=1
XC1[50] net16 outn sky130_fd_pr__cap_mim_m3_1 W=1 L=1 MF=1 m=1
XC1[49] net16 outn sky130_fd_pr__cap_mim_m3_1 W=1 L=1 MF=1 m=1
XC1[48] net16 outn sky130_fd_pr__cap_mim_m3_1 W=1 L=1 MF=1 m=1
XC1[47] net16 outn sky130_fd_pr__cap_mim_m3_1 W=1 L=1 MF=1 m=1
XC1[46] net16 outn sky130_fd_pr__cap_mim_m3_1 W=1 L=1 MF=1 m=1
XC1[45] net16 outn sky130_fd_pr__cap_mim_m3_1 W=1 L=1 MF=1 m=1
XC1[44] net16 outn sky130_fd_pr__cap_mim_m3_1 W=1 L=1 MF=1 m=1
XC1[43] net16 outn sky130_fd_pr__cap_mim_m3_1 W=1 L=1 MF=1 m=1
XC1[42] net16 outn sky130_fd_pr__cap_mim_m3_1 W=1 L=1 MF=1 m=1
XC1[41] net16 outn sky130_fd_pr__cap_mim_m3_1 W=1 L=1 MF=1 m=1
XC1[40] net16 outn sky130_fd_pr__cap_mim_m3_1 W=1 L=1 MF=1 m=1
XC1[39] net16 outn sky130_fd_pr__cap_mim_m3_1 W=1 L=1 MF=1 m=1
XC1[38] net16 outn sky130_fd_pr__cap_mim_m3_1 W=1 L=1 MF=1 m=1
XC1[37] net16 outn sky130_fd_pr__cap_mim_m3_1 W=1 L=1 MF=1 m=1
XC1[36] net16 outn sky130_fd_pr__cap_mim_m3_1 W=1 L=1 MF=1 m=1
XC1[35] net16 outn sky130_fd_pr__cap_mim_m3_1 W=1 L=1 MF=1 m=1
XC1[34] net16 outn sky130_fd_pr__cap_mim_m3_1 W=1 L=1 MF=1 m=1
XC1[33] net16 outn sky130_fd_pr__cap_mim_m3_1 W=1 L=1 MF=1 m=1
XC1[32] net16 outn sky130_fd_pr__cap_mim_m3_1 W=1 L=1 MF=1 m=1
XC1[31] net16 outn sky130_fd_pr__cap_mim_m3_1 W=1 L=1 MF=1 m=1
XC1[30] net16 outn sky130_fd_pr__cap_mim_m3_1 W=1 L=1 MF=1 m=1
XC1[29] net16 outn sky130_fd_pr__cap_mim_m3_1 W=1 L=1 MF=1 m=1
XC1[28] net16 outn sky130_fd_pr__cap_mim_m3_1 W=1 L=1 MF=1 m=1
XC1[27] net16 outn sky130_fd_pr__cap_mim_m3_1 W=1 L=1 MF=1 m=1
XC1[26] net16 outn sky130_fd_pr__cap_mim_m3_1 W=1 L=1 MF=1 m=1
XC1[25] net16 outn sky130_fd_pr__cap_mim_m3_1 W=1 L=1 MF=1 m=1
XC1[24] net16 outn sky130_fd_pr__cap_mim_m3_1 W=1 L=1 MF=1 m=1
XC1[23] net16 outn sky130_fd_pr__cap_mim_m3_1 W=1 L=1 MF=1 m=1
XC1[22] net16 outn sky130_fd_pr__cap_mim_m3_1 W=1 L=1 MF=1 m=1
XC1[21] net16 outn sky130_fd_pr__cap_mim_m3_1 W=1 L=1 MF=1 m=1
XC1[20] net16 outn sky130_fd_pr__cap_mim_m3_1 W=1 L=1 MF=1 m=1
XC1[19] net16 outn sky130_fd_pr__cap_mim_m3_1 W=1 L=1 MF=1 m=1
XC1[18] net16 outn sky130_fd_pr__cap_mim_m3_1 W=1 L=1 MF=1 m=1
XC1[17] net16 outn sky130_fd_pr__cap_mim_m3_1 W=1 L=1 MF=1 m=1
XC1[16] net16 outn sky130_fd_pr__cap_mim_m3_1 W=1 L=1 MF=1 m=1
XC1[15] net16 outn sky130_fd_pr__cap_mim_m3_1 W=1 L=1 MF=1 m=1
XC1[14] net16 outn sky130_fd_pr__cap_mim_m3_1 W=1 L=1 MF=1 m=1
XC1[13] net16 outn sky130_fd_pr__cap_mim_m3_1 W=1 L=1 MF=1 m=1
XC1[12] net16 outn sky130_fd_pr__cap_mim_m3_1 W=1 L=1 MF=1 m=1
XC1[11] net16 outn sky130_fd_pr__cap_mim_m3_1 W=1 L=1 MF=1 m=1
XC1[10] net16 outn sky130_fd_pr__cap_mim_m3_1 W=1 L=1 MF=1 m=1
XC1[9] net16 outn sky130_fd_pr__cap_mim_m3_1 W=1 L=1 MF=1 m=1
XC1[8] net16 outn sky130_fd_pr__cap_mim_m3_1 W=1 L=1 MF=1 m=1
XC1[7] net16 outn sky130_fd_pr__cap_mim_m3_1 W=1 L=1 MF=1 m=1
XC1[6] net16 outn sky130_fd_pr__cap_mim_m3_1 W=1 L=1 MF=1 m=1
XC1[5] net16 outn sky130_fd_pr__cap_mim_m3_1 W=1 L=1 MF=1 m=1
XC1[4] net16 outn sky130_fd_pr__cap_mim_m3_1 W=1 L=1 MF=1 m=1
XC1[3] net16 outn sky130_fd_pr__cap_mim_m3_1 W=1 L=1 MF=1 m=1
XC1[2] net16 outn sky130_fd_pr__cap_mim_m3_1 W=1 L=1 MF=1 m=1
XC1[1] net16 outn sky130_fd_pr__cap_mim_m3_1 W=1 L=1 MF=1 m=1
XC1[0] net16 outn sky130_fd_pr__cap_mim_m3_1 W=1 L=1 MF=1 m=1
XM8 net15 sw[7] net16 GND sky130_fd_pr__nfet_01v8_lvt L=0.15 W=1 nf=15 ad='int((nf+1)/2) * W/nf * 0.29'
+ as='int((nf+2)/2) * W/nf * 0.29' pd='2*int((nf+1)/2) * (W/nf + 0.29)' ps='2*int((nf+2)/2) * (W/nf + 0.29)'
+ nrd='0.29 / W' nrs='0.29 / W' sa=0 sb=0 sd=0 mult=1 m=1
**.ends
.end
